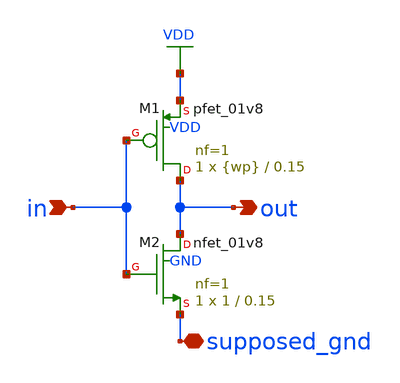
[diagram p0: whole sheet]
** sch_path: tut3/inv_nognd.sch
**.subckt inv_nognd in out supposed_gnd
*.ipin in
*.opin out
*.iopin supposed_gnd
XM1 out in VDD VDD sky130_fd_pr__pfet_01v8 L=0.15 W={wp} nf=1 ad='int((nf+1)/2) * W/nf * 0.29' as='int((nf+2)/2) * W/nf * 0.29'
+ pd='2*int((nf+1)/2) * (W/nf + 0.29)' ps='2*int((nf+2)/2) * (W/nf + 0.29)' nrd='0.29 / W' nrs='0.29 / W'
+ sa=0 sb=0 sd=0 mult=1 m=1
XM2 out in supposed_gnd GND sky130_fd_pr__nfet_01v8 L=0.15 W=1 nf=1 ad='int((nf+1)/2) * W/nf * 0.29'
+ as='int((nf+2)/2) * W/nf * 0.29' pd='2*int((nf+1)/2) * (W/nf + 0.29)' ps='2*int((nf+2)/2) * (W/nf + 0.29)'
+ nrd='0.29 / W' nrs='0.29 / W' sa=0 sb=0 sd=0 mult=1 m=1
**.ends
.GLOBAL VDD
.end
